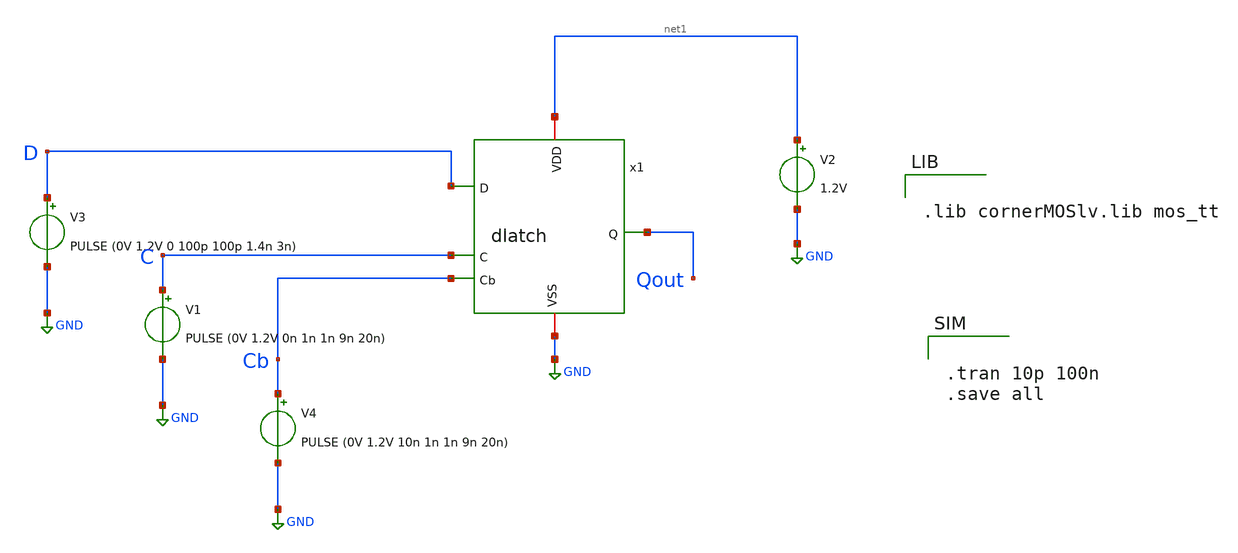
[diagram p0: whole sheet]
** sch_path: dlatch-testbench.sch
**.subckt dlatch-testbench
x1 net1 C Cb D Qout GND dlatch
V2 net1 GND 1.2V
V3 D GND PULSE (0V 1.2V 0 100p 100p 1.4n 3n)
V1 C GND PULSE (0V 1.2V 0n 1n 1n 9n 20n)
V4 Cb GND PULSE (0V 1.2V 10n 1n 1n 9n 20n)
**** begin user architecture code


.tran 10p 100n
.save all




.lib cornerMOSlv.lib mos_tt

**** end user architecture code
**.ends

* expanding   symbol:  xchem/xchem/dlatch.sym # of pins=6
** sym_path: dlatch.sym
** sch_path: dlatch.sch
.subckt dlatch VDD C Cb D Q VSS
*.ipin C
*.ipin Cb
*.ipin D
*.opin Q
*.iopin VDD
*.iopin VSS
x1 VDD net2 net1 C Cb VSS D mux
x2 VDD net1 Q VSS inverter
x3 VDD Q net2 VSS inverter
.ends


* expanding   symbol:  xchem/xchem/mux.sym # of pins=7
** sym_path: mux.sym
** sch_path: mux.sch
.subckt mux VDD D1 Y S Sb VSS D0
*.ipin S
*.ipin Sb
*.ipin D0
*.ipin D1
*.iopin VDD
*.iopin VSS
*.iopin Y
XM1 Y Sb D1 VDD sg13_lv_pmos w=0.15u l=0.13u ng=1 m=1 mm_ok=1
XM2 D0 S Y VDD sg13_lv_pmos w=0.15u l=0.13u ng=1 m=1 mm_ok=1
XM3 Y S D1 VSS sg13_lv_nmos w=0.15u l=0.13u ng=1 m=1 mm_ok=1
XM4 D0 Sb Y VSS sg13_lv_nmos w=0.15u l=0.13u ng=1 m=1 mm_ok=1
.ends


* expanding   symbol:  xchem/xchem/inverter.sym # of pins=4
** sym_path: inverter.sym
** sch_path: inverter.sch
.subckt inverter VDD A Y VSS
*.ipin A
*.iopin VDD
*.iopin VSS
*.opin Y
XM1 Y A VDD VDD sg13_lv_pmos w=0.15u l=0.13u ng=1 m=1 mm_ok=1
XM2 Y A VSS VSS sg13_lv_nmos w=0.15u l=0.13u ng=1 m=1 mm_ok=1
.ends

.GLOBAL GND
.end
